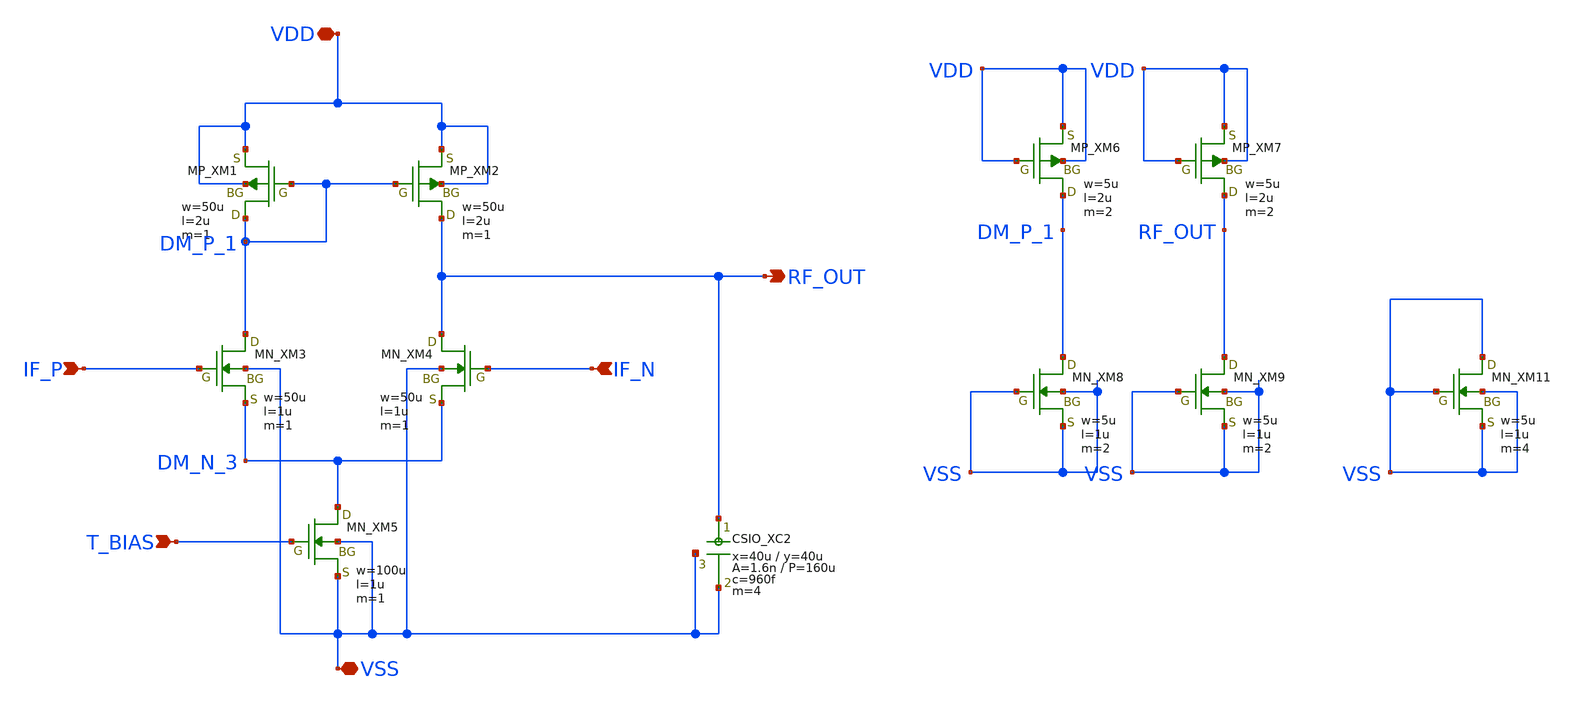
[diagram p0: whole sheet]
** sch_path: member_project/MIXER/noritsuna/xschem/diff_amp.sch
**.subckt diff_amp IF_P IF_N T_BIAS VDD VSS RF_OUT
*.ipin IF_P
*.ipin IF_N
*.ipin T_BIAS
*.iopin VDD
*.iopin VSS
*.opin RF_OUT
XXM1 DM_P_1 DM_P_1 VDD VDD PMOS w=50u l=2u nrd=0 nrs=0 m=1
XXM2 RF_OUT DM_P_1 VDD VDD PMOS w=50u l=2u nrd=0 nrs=0 m=1
XXM3 DM_P_1 IF_P DM_N_3 VSS NMOS w=50u l=1u nrd=0 nrs=0 m=1
XXM4 RF_OUT IF_N DM_N_3 VSS NMOS w=50u l=1u nrd=0 nrs=0 m=1
XXM5 DM_N_3 T_BIAS VSS VSS NMOS w=100u l=1u nrd=0 nrs=0 m=1
XXC2 RF_OUT VSS VSS F_CSIO c=960f x=40u y=40u m=4
XXM6 DM_P_1 VDD VDD VDD PMOS w=5u l=2u nrd=0 nrs=0 m=2
XXM7 RF_OUT VDD VDD VDD PMOS w=5u l=2u nrd=0 nrs=0 m=2
XXM8 DM_P_1 VSS VSS VSS NMOS w=5u l=1u nrd=0 nrs=0 m=2
XXM11 VSS VSS VSS VSS NMOS w=5u l=1u nrd=0 nrs=0 m=4
XXM9 RF_OUT VSS VSS VSS NMOS w=5u l=1u nrd=0 nrs=0 m=2
**.ends
.end
